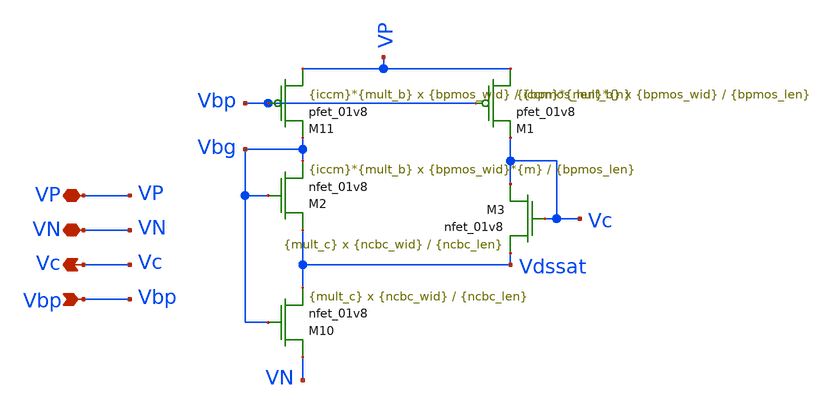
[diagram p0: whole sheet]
** sch_path: Circuits, Symbols, Extras/ncbc.sch
**.subckt ncbc VP VN Vc Vbp
*.iopin VP
*.iopin VN
*.opin Vc
*.ipin Vbp
XM10 VN Vbg Vdssat VN sky130_fd_pr__nfet_01v8 L={ncbc_len} W={ncbc_wid} nf=1 ad='int((nf+1)/2) * W/nf * 0.29'
+ as='int((nf+2)/2) * W/nf * 0.29' pd='2*int((nf+1)/2) * (W/nf + 0.29)' ps='2*int((nf+2)/2) * (W/nf + 0.29)'
+ nrd='0.29 / W' nrs='0.29 / W' sa=0 sb=0 sd=0 mult={mult_c} m={mult_c}
XM11 VP Vbp Vbg VP sky130_fd_pr__pfet_01v8 L={bpmos_len}*{n} W={bpmos_wid} nf=1 ad='int((nf+1)/2) * W/nf * 0.29'
+ as='int((nf+2)/2) * W/nf * 0.29' pd='2*int((nf+1)/2) * (W/nf + 0.29)' ps='2*int((nf+2)/2) * (W/nf + 0.29)'
+ nrd='0.29 / W' nrs='0.29 / W' sa=0 sb=0 sd=0 mult={iccm}*{mult_b} m={iccm}*{mult_b}
XM1 VP Vbp Vc VP sky130_fd_pr__pfet_01v8 L={bpmos_len} W={bpmos_wid} nf=1 ad='int((nf+1)/2) * W/nf * 0.29'
+ as='int((nf+2)/2) * W/nf * 0.29' pd='2*int((nf+1)/2) * (W/nf + 0.29)' ps='2*int((nf+2)/2) * (W/nf + 0.29)'
+ nrd='0.29 / W' nrs='0.29 / W' sa=0 sb=0 sd=0 mult={iccm}*{mult_b} m={iccm}*{mult_b}
XM2 Vdssat Vbg Vbg VN sky130_fd_pr__nfet_01v8 L={bpmos_len} W={bpmos_wid}*{m} nf=1 ad='int((nf+1)/2) * W/nf * 0.29'
+ as='int((nf+2)/2) * W/nf * 0.29' pd='2*int((nf+1)/2) * (W/nf + 0.29)' ps='2*int((nf+2)/2) * (W/nf + 0.29)'
+ nrd='0.29 / W' nrs='0.29 / W' sa=0 sb=0 sd=0 mult={iccm}*{mult_b} m={iccm}*{mult_b}
XM3 Vc Vc Vdssat VN sky130_fd_pr__nfet_01v8 L={ncbc_len} W={ncbc_wid} nf=1 ad='int((nf+1)/2) * W/nf * 0.29'
+ as='int((nf+2)/2) * W/nf * 0.29' pd='2*int((nf+1)/2) * (W/nf + 0.29)' ps='2*int((nf+2)/2) * (W/nf + 0.29)'
+ nrd='0.29 / W' nrs='0.29 / W' sa=0 sb=0 sd=0 mult={mult_c} m={mult_c}
**.ends
.end
